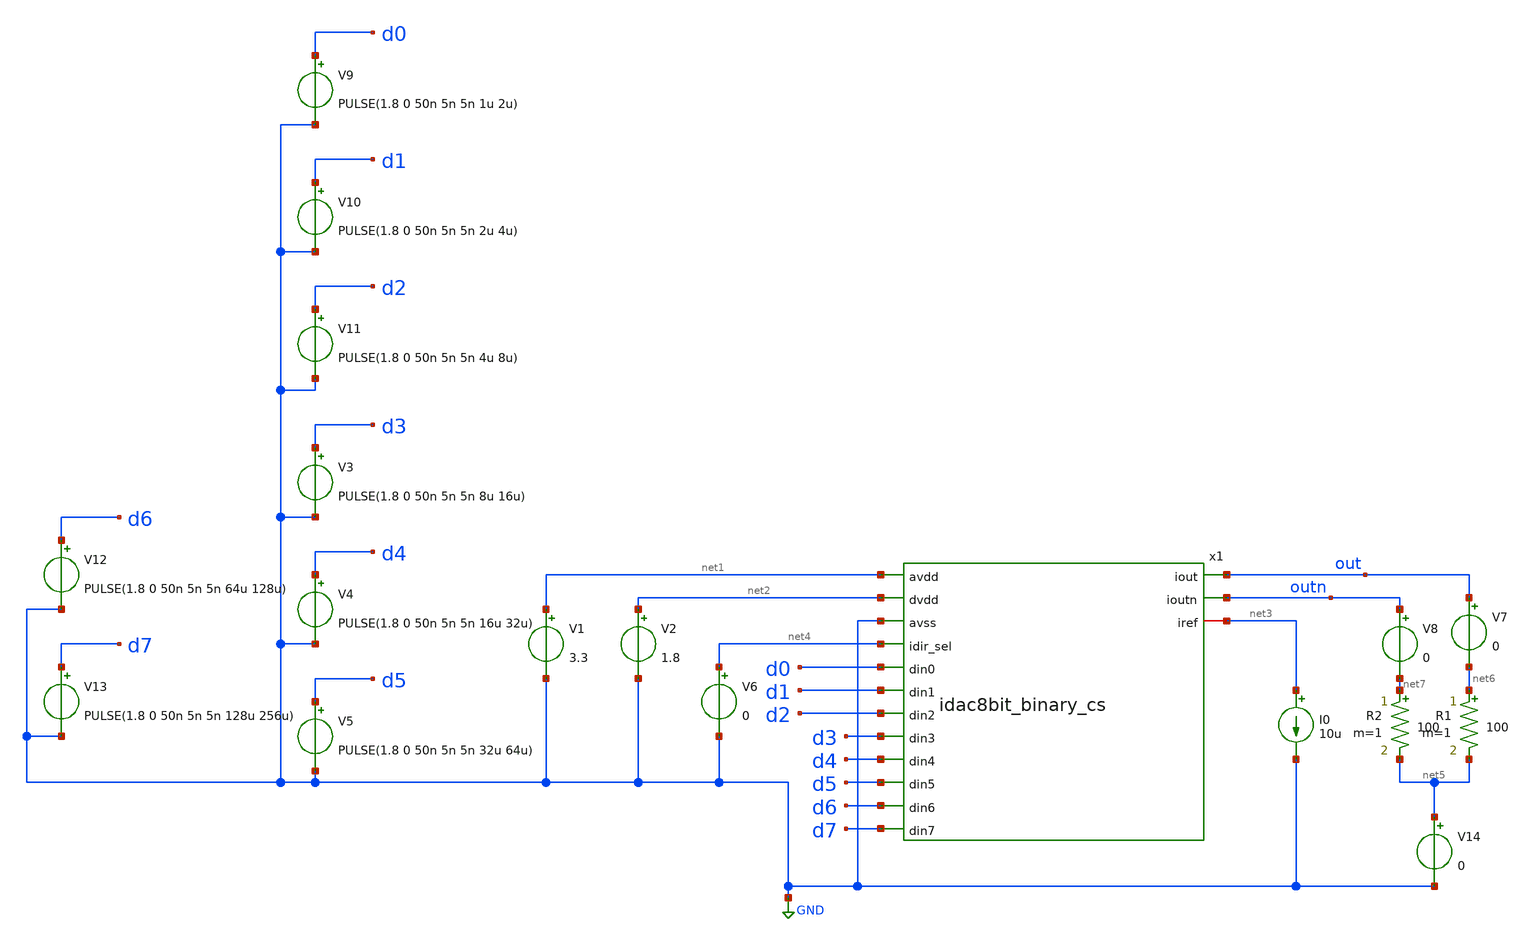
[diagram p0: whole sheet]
** sch_path: xschem/idac8bit_cs_tb.sch
**.subckt idac8bit_cs_tb
V1 net1 GND 3.3
V2 net2 GND 1.8
I0 net3 GND 10u
V3 d3 GND PULSE(1.8 0 50n 5n 5n 8u 16u)
V4 d4 GND PULSE(1.8 0 50n 5n 5n 16u 32u)
V5 d5 GND PULSE(1.8 0 50n 5n 5n 32u 64u)
V6 net4 GND 0
V7 out net6 0
R1 net6 net5 100 m=1
V8 outn net7 0
R2 net7 net5 100 m=1
V9 d0 GND PULSE(1.8 0 50n 5n 5n 1u 2u)
V10 d1 GND PULSE(1.8 0 50n 5n 5n 2u 4u)
V11 d2 GND PULSE(1.8 0 50n 5n 5n 4u 8u)
x1 net1 net2 out outn d0 net4 d1 GND d2 d3 net3 d4 d5 d6 d7 idac8bit_binary_cs
V12 d6 GND PULSE(1.8 0 50n 5n 5n 64u 128u)
V13 d7 GND PULSE(1.8 0 50n 5n 5n 128u 256u)
V14 net5 GND 0
**** begin user architecture code
 .lib $::SKYWATER_MODELS/sky130.lib.spice tt
.include $::SKYWATER_STDCELLS/../../sky130_fd_sc_hvl/spice/sky130_fd_sc_hvl.spice

.param mc_mm_switch=0
.param mc_pr_switch=1



.option wnflag=0
.save v(out) v(outn) i(V8) i(V7)
.control
tran 100n 256u
plot v(out)
plot i(V7)
write currentmirrortb.raw
op
.endc


**** end user architecture code
**.ends
.GLOBAL GND
.end
